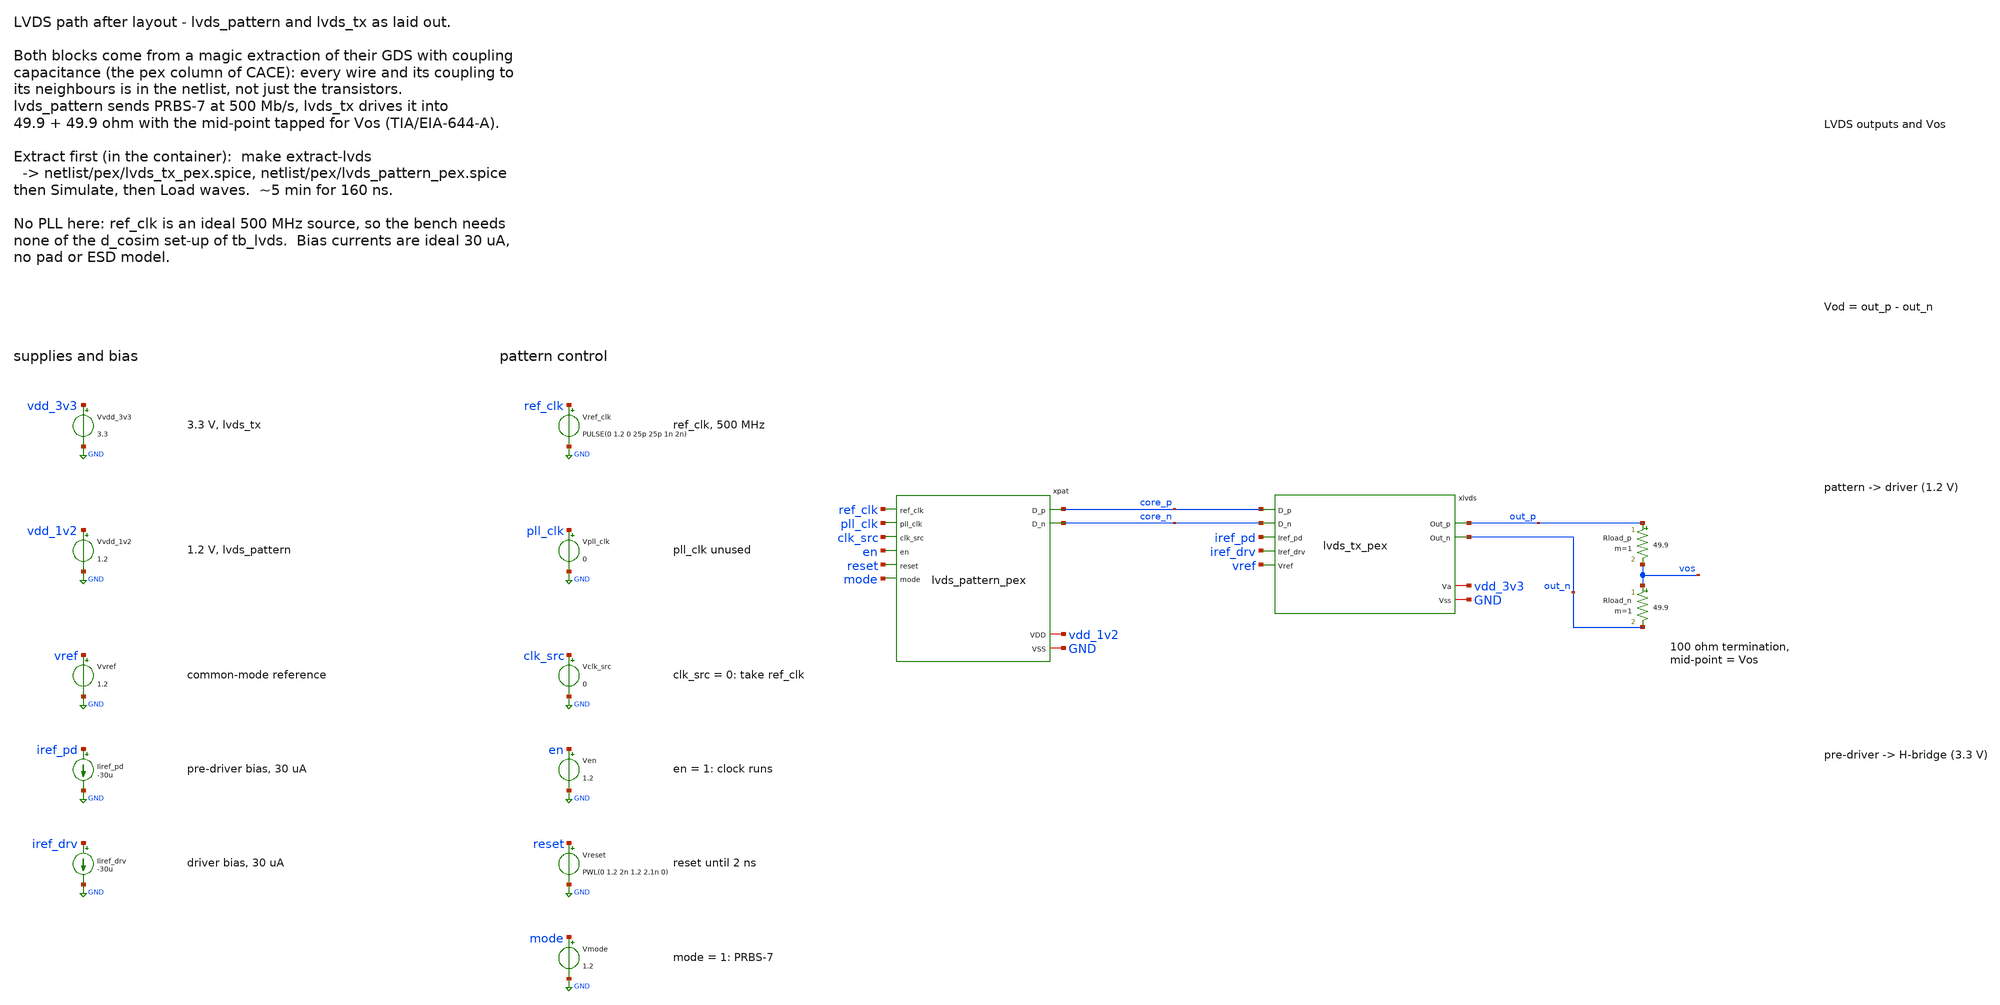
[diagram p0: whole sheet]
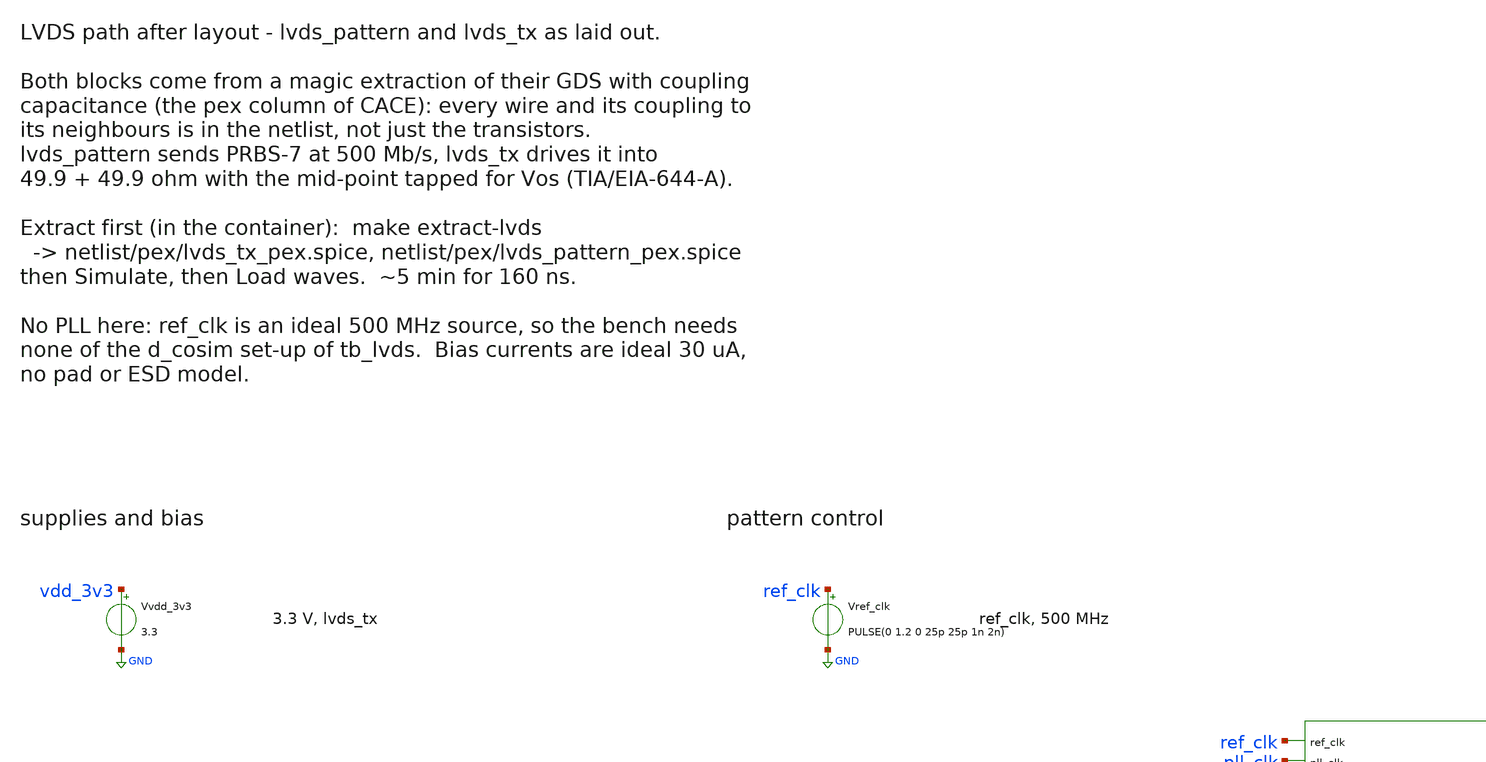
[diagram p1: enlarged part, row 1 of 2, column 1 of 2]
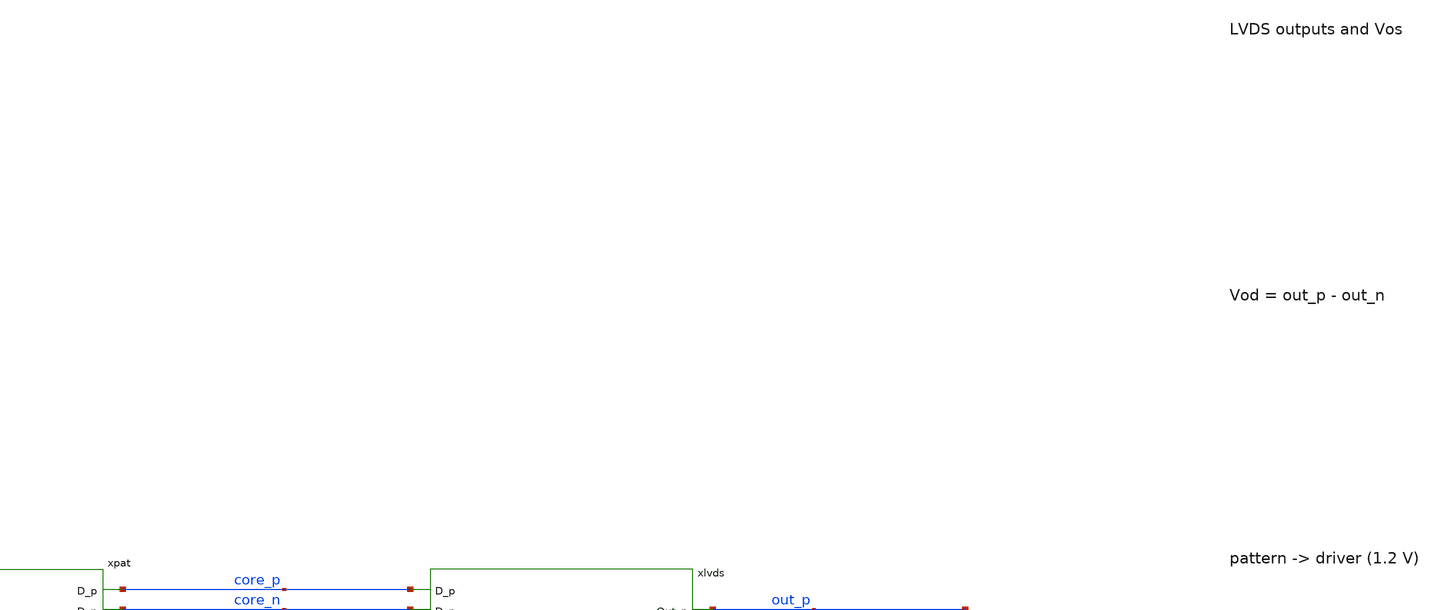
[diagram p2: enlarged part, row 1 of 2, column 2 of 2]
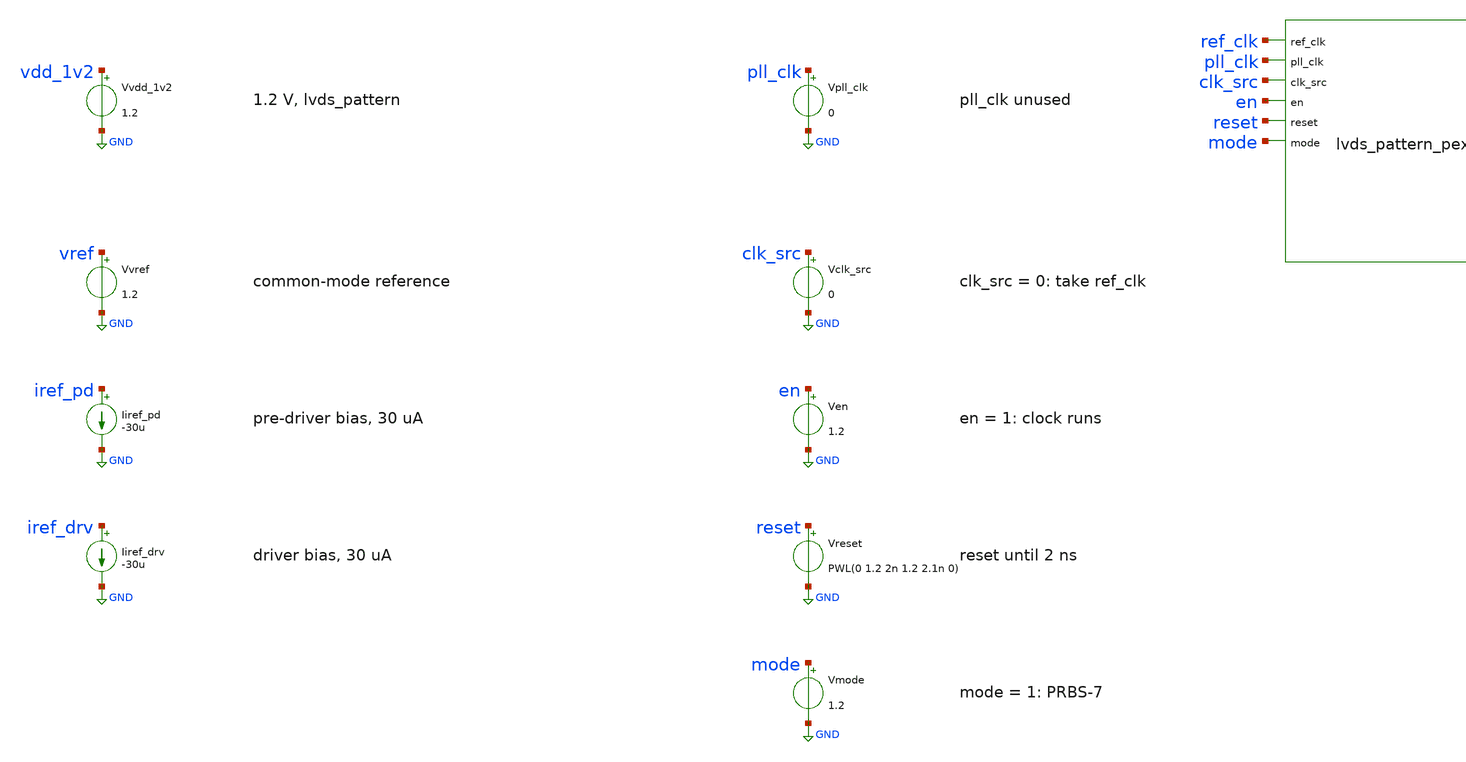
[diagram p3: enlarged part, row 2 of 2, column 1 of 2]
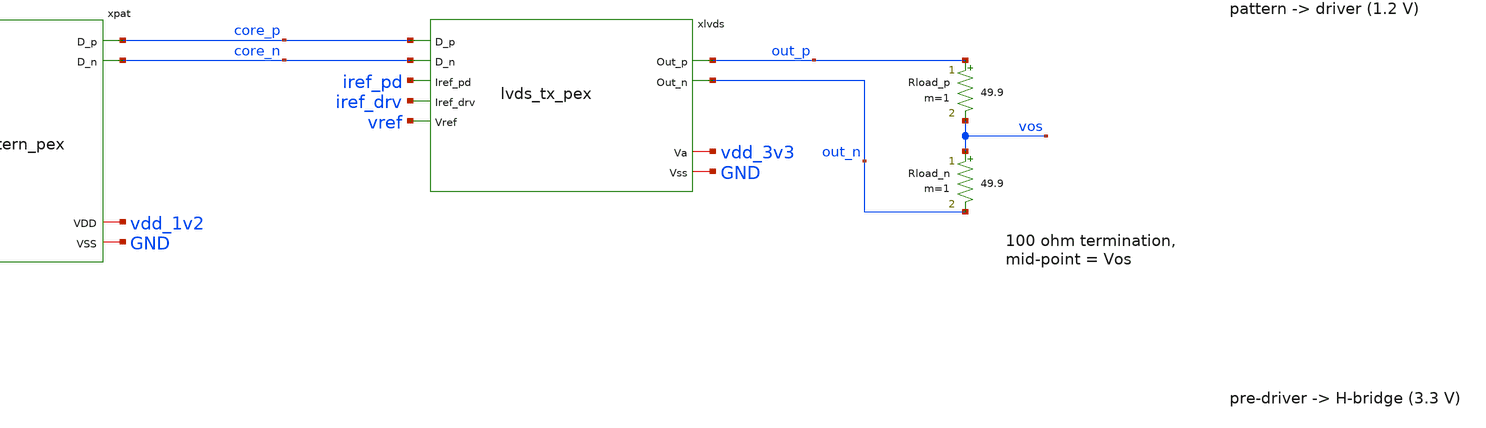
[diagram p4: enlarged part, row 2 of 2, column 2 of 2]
** sch_path: testbenches/xschem/sg13cmos5l_chipalooza_analog_project_tb_lvds_postlayout.sch
**.subckt sg13cmos5l_chipalooza_analog_project_tb_lvds_postlayout
Vvdd_3v3 vdd_3v3 GND 3.3
Vvdd_1v2 vdd_1v2 GND 1.2
Vvref vref GND 1.2
Iiref_pd iref_pd GND -30u
Iiref_drv iref_drv GND -30u
Vref_clk ref_clk GND PULSE(0 1.2 0 25p 25p 1n 2n)
Vpll_clk pll_clk GND 0
Vclk_src clk_src GND 0
Ven en GND 1.2
Vreset reset GND PWL(0 1.2 2n 1.2 2.1n 0)
Vmode mode GND 1.2
xpat ref_clk pll_clk clk_src en reset mode core_p core_n vdd_1v2 GND lvds_pattern
xlvds core_p core_n iref_pd iref_drv vref vdd_3v3 out_p out_n GND lvds_tx
Rload_p out_p vos 49.9 m=1
Rload_n vos out_n 49.9 m=1
**** begin user architecture code


.lib cornerMOSlv.lib mos_tt
.lib cornerMOShv.lib mos_tt
.lib cornerRES.lib res_typ
.lib cornerDIO.lib dio_tt
.include cap_cmomf.lib
* the two extracted blocks (make extract-lvds); the paths are relative to
* testbenches/xschem/simulations, where xschem runs ngspice
.include ../../../netlist/pex/lvds_tx_pex.spice
.include ../../../netlist/pex/lvds_pattern_pex.spice
.temp 27
.options klu method=trap reltol=1e-3 abstol=1e-12 gmin=1e-12
* the common-mode loop starts near its operating point instead of
* climbing out of the rail for ~60 ns
.ic v(xlvds.xdrv.cmfb)=1.54
.control
save out_p out_n vos core_p core_n ref_clk xlvds.in_p xlvds.in_n
tran 10p 160n 0 10p
let vod = v(out_p) - v(out_n)
* TIA/EIA-644-A on the settled part: |Vod| 247..454 mV, Vos 1.125..1.375 V,
* Vos peak-to-peak <= 150 mV
meas tran vod_max MAX vod from=60n to=160n
meas tran vod_min MIN vod from=60n to=160n
meas tran vos_avg AVG v(vos) from=60n to=160n
meas tran vos_max MAX v(vos) from=60n to=160n
meas tran vos_min MIN v(vos) from=60n to=160n
let vos_pp = vos_max - vos_min
print vod_max vod_min vos_avg vos_pp
write sg13cmos5l_chipalooza_analog_project_tb_lvds_postlayout.raw
.endc


**** end user architecture code
**.ends
.GLOBAL GND
.end
